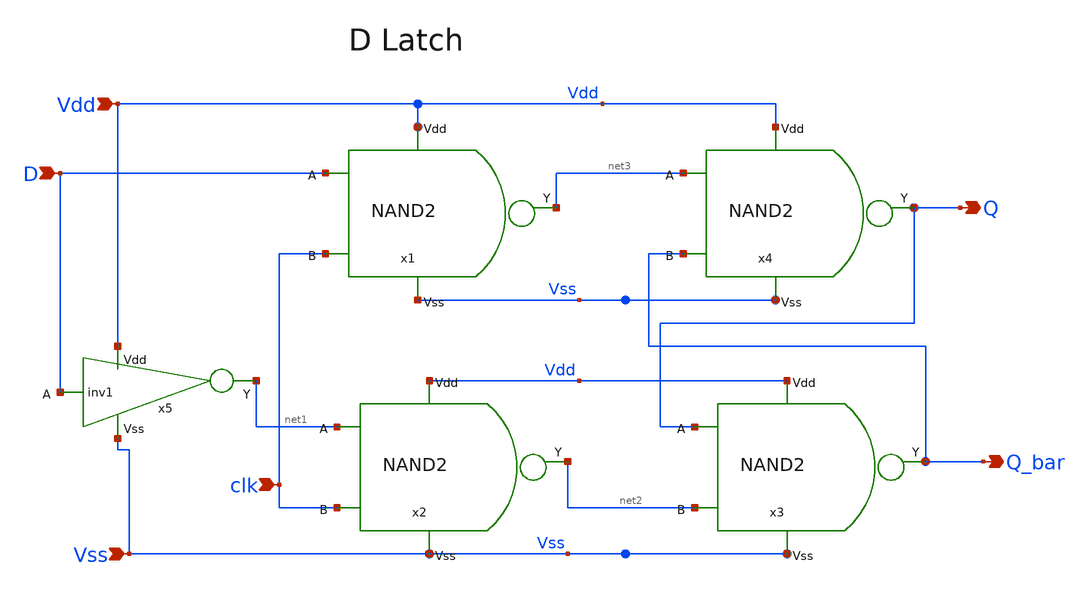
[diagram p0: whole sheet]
** sch_path: designs/libs/core_digital/schem/D_latch1.sch
**.subckt D_latch1 D Vdd Vss clk Q Q_bar
*.ipin D
*.ipin Vdd
*.ipin Vss
*.ipin clk
*.opin Q
*.opin Q_bar
x1 Vdd net3 D clk Vss NAND2
x2 Vdd net2 net1 clk Vss NAND2
x3 Vdd Q_bar Q net2 Vss NAND2
x4 Vdd Q net3 Q_bar Vss NAND2
x5 Vdd D net1 Vss inv1
**.ends
.end
